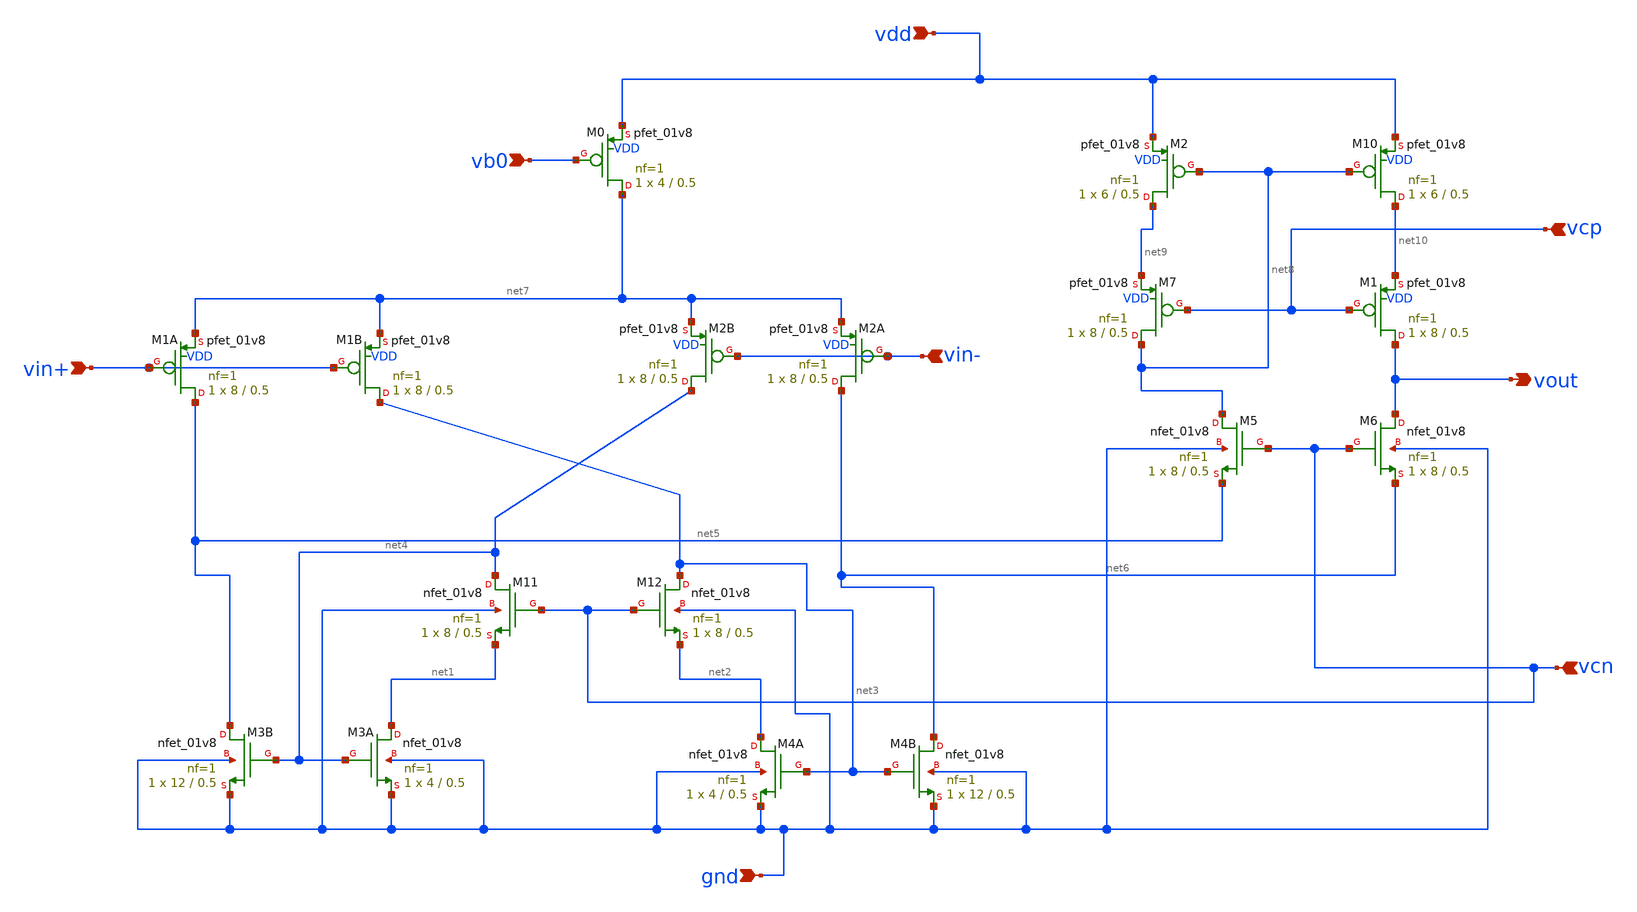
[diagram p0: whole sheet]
** sch_path: schematic/conv.sch
**.subckt conv vdd vin+ vin- vb0 vcn vcp gnd vout
*.ipin vdd
*.ipin vin+
*.ipin vin-
*.ipin vb0
*.ipin vcn
*.ipin vcp
*.ipin gnd
*.opin vout
XM3A net1 net4 gnd gnd sky130_fd_pr__nfet_01v8 L=0.5 W=4 nf=1 ad='int((nf+1)/2) * W/nf * 0.29' as='int((nf+2)/2) * W/nf * 0.29'
+ pd='2*int((nf+1)/2) * (W/nf + 0.29)' ps='2*int((nf+2)/2) * (W/nf + 0.29)' nrd='0.29 / W' nrs='0.29 / W'
+ sa=0 sb=0 sd=0 mult=1 m=1
XM3B net5 net4 gnd gnd sky130_fd_pr__nfet_01v8 L=0.5 W=12 nf=1 ad='int((nf+1)/2) * W/nf * 0.29' as='int((nf+2)/2) * W/nf * 0.29'
+ pd='2*int((nf+1)/2) * (W/nf + 0.29)' ps='2*int((nf+2)/2) * (W/nf + 0.29)' nrd='0.29 / W' nrs='0.29 / W'
+ sa=0 sb=0 sd=0 mult=1 m=1
XM4A net2 net3 gnd gnd sky130_fd_pr__nfet_01v8 L=0.5 W=4 nf=1 ad='int((nf+1)/2) * W/nf * 0.29' as='int((nf+2)/2) * W/nf * 0.29'
+ pd='2*int((nf+1)/2) * (W/nf + 0.29)' ps='2*int((nf+2)/2) * (W/nf + 0.29)' nrd='0.29 / W' nrs='0.29 / W'
+ sa=0 sb=0 sd=0 mult=1 m=1
XM4B net6 net3 gnd gnd sky130_fd_pr__nfet_01v8 L=0.5 W=12 nf=1 ad='int((nf+1)/2) * W/nf * 0.29' as='int((nf+2)/2) * W/nf * 0.29'
+ pd='2*int((nf+1)/2) * (W/nf + 0.29)' ps='2*int((nf+2)/2) * (W/nf + 0.29)' nrd='0.29 / W' nrs='0.29 / W'
+ sa=0 sb=0 sd=0 mult=1 m=1
XM5 net8 vcn net5 gnd sky130_fd_pr__nfet_01v8 L=0.5 W=8 nf=1 ad='int((nf+1)/2) * W/nf * 0.29' as='int((nf+2)/2) * W/nf * 0.29'
+ pd='2*int((nf+1)/2) * (W/nf + 0.29)' ps='2*int((nf+2)/2) * (W/nf + 0.29)' nrd='0.29 / W' nrs='0.29 / W'
+ sa=0 sb=0 sd=0 mult=1 m=1
XM6 vout vcn net6 gnd sky130_fd_pr__nfet_01v8 L=0.5 W=8 nf=1 ad='int((nf+1)/2) * W/nf * 0.29' as='int((nf+2)/2) * W/nf * 0.29'
+ pd='2*int((nf+1)/2) * (W/nf + 0.29)' ps='2*int((nf+2)/2) * (W/nf + 0.29)' nrd='0.29 / W' nrs='0.29 / W'
+ sa=0 sb=0 sd=0 mult=1 m=1
XM12 net3 vcn net2 gnd sky130_fd_pr__nfet_01v8 L=0.5 W=8 nf=1 ad='int((nf+1)/2) * W/nf * 0.29' as='int((nf+2)/2) * W/nf * 0.29'
+ pd='2*int((nf+1)/2) * (W/nf + 0.29)' ps='2*int((nf+2)/2) * (W/nf + 0.29)' nrd='0.29 / W' nrs='0.29 / W'
+ sa=0 sb=0 sd=0 mult=1 m=1
XM11 net4 vcn net1 gnd sky130_fd_pr__nfet_01v8 L=0.5 W=8 nf=1 ad='int((nf+1)/2) * W/nf * 0.29' as='int((nf+2)/2) * W/nf * 0.29'
+ pd='2*int((nf+1)/2) * (W/nf + 0.29)' ps='2*int((nf+2)/2) * (W/nf + 0.29)' nrd='0.29 / W' nrs='0.29 / W'
+ sa=0 sb=0 sd=0 mult=1 m=1
XM1B net3 vin+ net7 VDD sky130_fd_pr__pfet_01v8 L=0.5 W=8 nf=1 ad='int((nf+1)/2) * W/nf * 0.29' as='int((nf+2)/2) * W/nf * 0.29'
+ pd='2*int((nf+1)/2) * (W/nf + 0.29)' ps='2*int((nf+2)/2) * (W/nf + 0.29)' nrd='0.29 / W' nrs='0.29 / W'
+ sa=0 sb=0 sd=0 mult=1 m=1
XM1A net5 vin+ net7 VDD sky130_fd_pr__pfet_01v8 L=0.5 W=8 nf=1 ad='int((nf+1)/2) * W/nf * 0.29' as='int((nf+2)/2) * W/nf * 0.29'
+ pd='2*int((nf+1)/2) * (W/nf + 0.29)' ps='2*int((nf+2)/2) * (W/nf + 0.29)' nrd='0.29 / W' nrs='0.29 / W'
+ sa=0 sb=0 sd=0 mult=1 m=1
XM2 net9 net8 vdd VDD sky130_fd_pr__pfet_01v8 L=0.5 W=6 nf=1 ad='int((nf+1)/2) * W/nf * 0.29' as='int((nf+2)/2) * W/nf * 0.29'
+ pd='2*int((nf+1)/2) * (W/nf + 0.29)' ps='2*int((nf+2)/2) * (W/nf + 0.29)' nrd='0.29 / W' nrs='0.29 / W'
+ sa=0 sb=0 sd=0 mult=1 m=1
XM7 net8 vcp net9 VDD sky130_fd_pr__pfet_01v8 L=0.5 W=8 nf=1 ad='int((nf+1)/2) * W/nf * 0.29' as='int((nf+2)/2) * W/nf * 0.29'
+ pd='2*int((nf+1)/2) * (W/nf + 0.29)' ps='2*int((nf+2)/2) * (W/nf + 0.29)' nrd='0.29 / W' nrs='0.29 / W'
+ sa=0 sb=0 sd=0 mult=1 m=1
XM1 vout vcp net10 VDD sky130_fd_pr__pfet_01v8 L=0.5 W=8 nf=1 ad='int((nf+1)/2) * W/nf * 0.29' as='int((nf+2)/2) * W/nf * 0.29'
+ pd='2*int((nf+1)/2) * (W/nf + 0.29)' ps='2*int((nf+2)/2) * (W/nf + 0.29)' nrd='0.29 / W' nrs='0.29 / W'
+ sa=0 sb=0 sd=0 mult=1 m=1
XM0 net7 vb0 vdd VDD sky130_fd_pr__pfet_01v8 L=0.5 W=4 nf=1 ad='int((nf+1)/2) * W/nf * 0.29' as='int((nf+2)/2) * W/nf * 0.29'
+ pd='2*int((nf+1)/2) * (W/nf + 0.29)' ps='2*int((nf+2)/2) * (W/nf + 0.29)' nrd='0.29 / W' nrs='0.29 / W'
+ sa=0 sb=0 sd=0 mult=1 m=1
XM2B net4 vin- net7 VDD sky130_fd_pr__pfet_01v8 L=0.5 W=8 nf=1 ad='int((nf+1)/2) * W/nf * 0.29' as='int((nf+2)/2) * W/nf * 0.29'
+ pd='2*int((nf+1)/2) * (W/nf + 0.29)' ps='2*int((nf+2)/2) * (W/nf + 0.29)' nrd='0.29 / W' nrs='0.29 / W'
+ sa=0 sb=0 sd=0 mult=1 m=1
XM10 net10 net8 vdd VDD sky130_fd_pr__pfet_01v8 L=0.5 W=6 nf=1 ad='int((nf+1)/2) * W/nf * 0.29' as='int((nf+2)/2) * W/nf * 0.29'
+ pd='2*int((nf+1)/2) * (W/nf + 0.29)' ps='2*int((nf+2)/2) * (W/nf + 0.29)' nrd='0.29 / W' nrs='0.29 / W'
+ sa=0 sb=0 sd=0 mult=1 m=1
XM2A net6 vin- net7 VDD sky130_fd_pr__pfet_01v8 L=0.5 W=8 nf=1 ad='int((nf+1)/2) * W/nf * 0.29' as='int((nf+2)/2) * W/nf * 0.29'
+ pd='2*int((nf+1)/2) * (W/nf + 0.29)' ps='2*int((nf+2)/2) * (W/nf + 0.29)' nrd='0.29 / W' nrs='0.29 / W'
+ sa=0 sb=0 sd=0 mult=1 m=1
**.ends
.end
